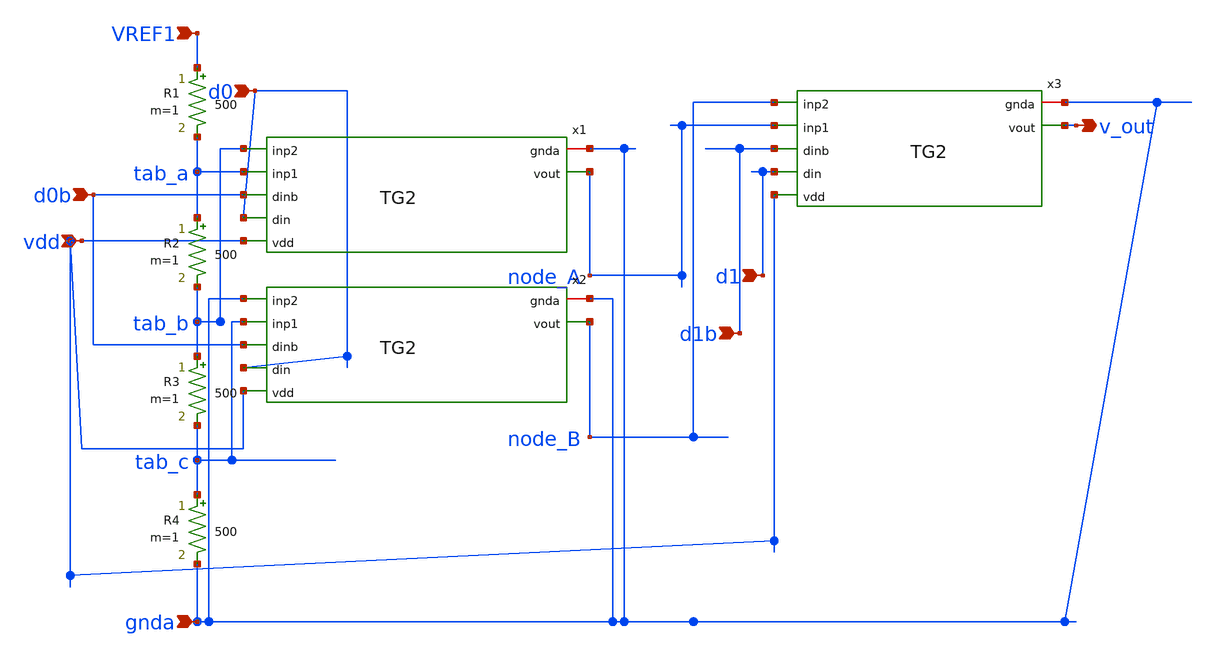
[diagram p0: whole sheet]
** sch_path: week_4/2bitdac/2bitdac.sch
**.subckt 2bitdac VREF1 gnda d0 d0b vdd d1 v_out d1b
*.ipin VREF1
*.ipin gnda
*.ipin d0
*.ipin d0b
*.ipin vdd
*.ipin d1
*.opin v_out
*.ipin d1b
R1 VREF1 tab_a 500 m=1
R2 tab_a tab_b 500 m=1
R3 tab_b tab_c 500 m=1
R4 tab_c gnda 500 m=1
Xx1 gnda node_A tab_b tab_a d0b d0 vdd TG2
Xx2 gnda node_B gnda tab_c d0b d0 vdd TG2
Xx3 gnda v_out node_B node_A d1b d1 vdd TG2
**.ends

* expanding   symbol:  xschem/TG2.sym # of pins=7
** sym_path: prelayout/TG2.sym
** sch_path: prelayout/TG2.sch
.subckt TG2 gnda vout inp2 inp1 dinb din vdd
*.ipin din
*.ipin inp1
*.ipin inp2
*.ipin vdd
*.opin vout
*.iopin gnda
*.ipin dinb
XM1 vout din inp1 gnda sky130_fd_pr__nfet_01v8 L=0.15 W=1 nf=1 ad=0.3 as=0.3 pd=1.68 ps=1.68 nrd=0.3
+ nrs=0.3 sa=0 sb=0 sd=0 mult=1 m=1
XM2 vout dinb inp1 vdd sky130_fd_pr__pfet_01v8 L=0.15 W=1 nf=1 ad=0.3 as=0.3 pd=1.68 ps=1.68 nrd=0.3
+ nrs=0.3 sa=0 sb=0 sd=0 mult=1 m=1
XM7 vout dinb inp2 gnda sky130_fd_pr__nfet_01v8 L=0.15 W=1 nf=1 ad=0.3 as=0.3 pd=1.68 ps=1.68
+ nrd=0.3 nrs=0.3 sa=0 sb=0 sd=0 mult=1 m=1
XM8 vout din inp2 vdd sky130_fd_pr__pfet_01v8 L=0.15 W=1 nf=1 ad=0.3 as=0.3 pd=1.68 ps=1.68 nrd=0.3
+ nrs=0.3 sa=0 sb=0 sd=0 mult=1 m=1
.ends

.end
